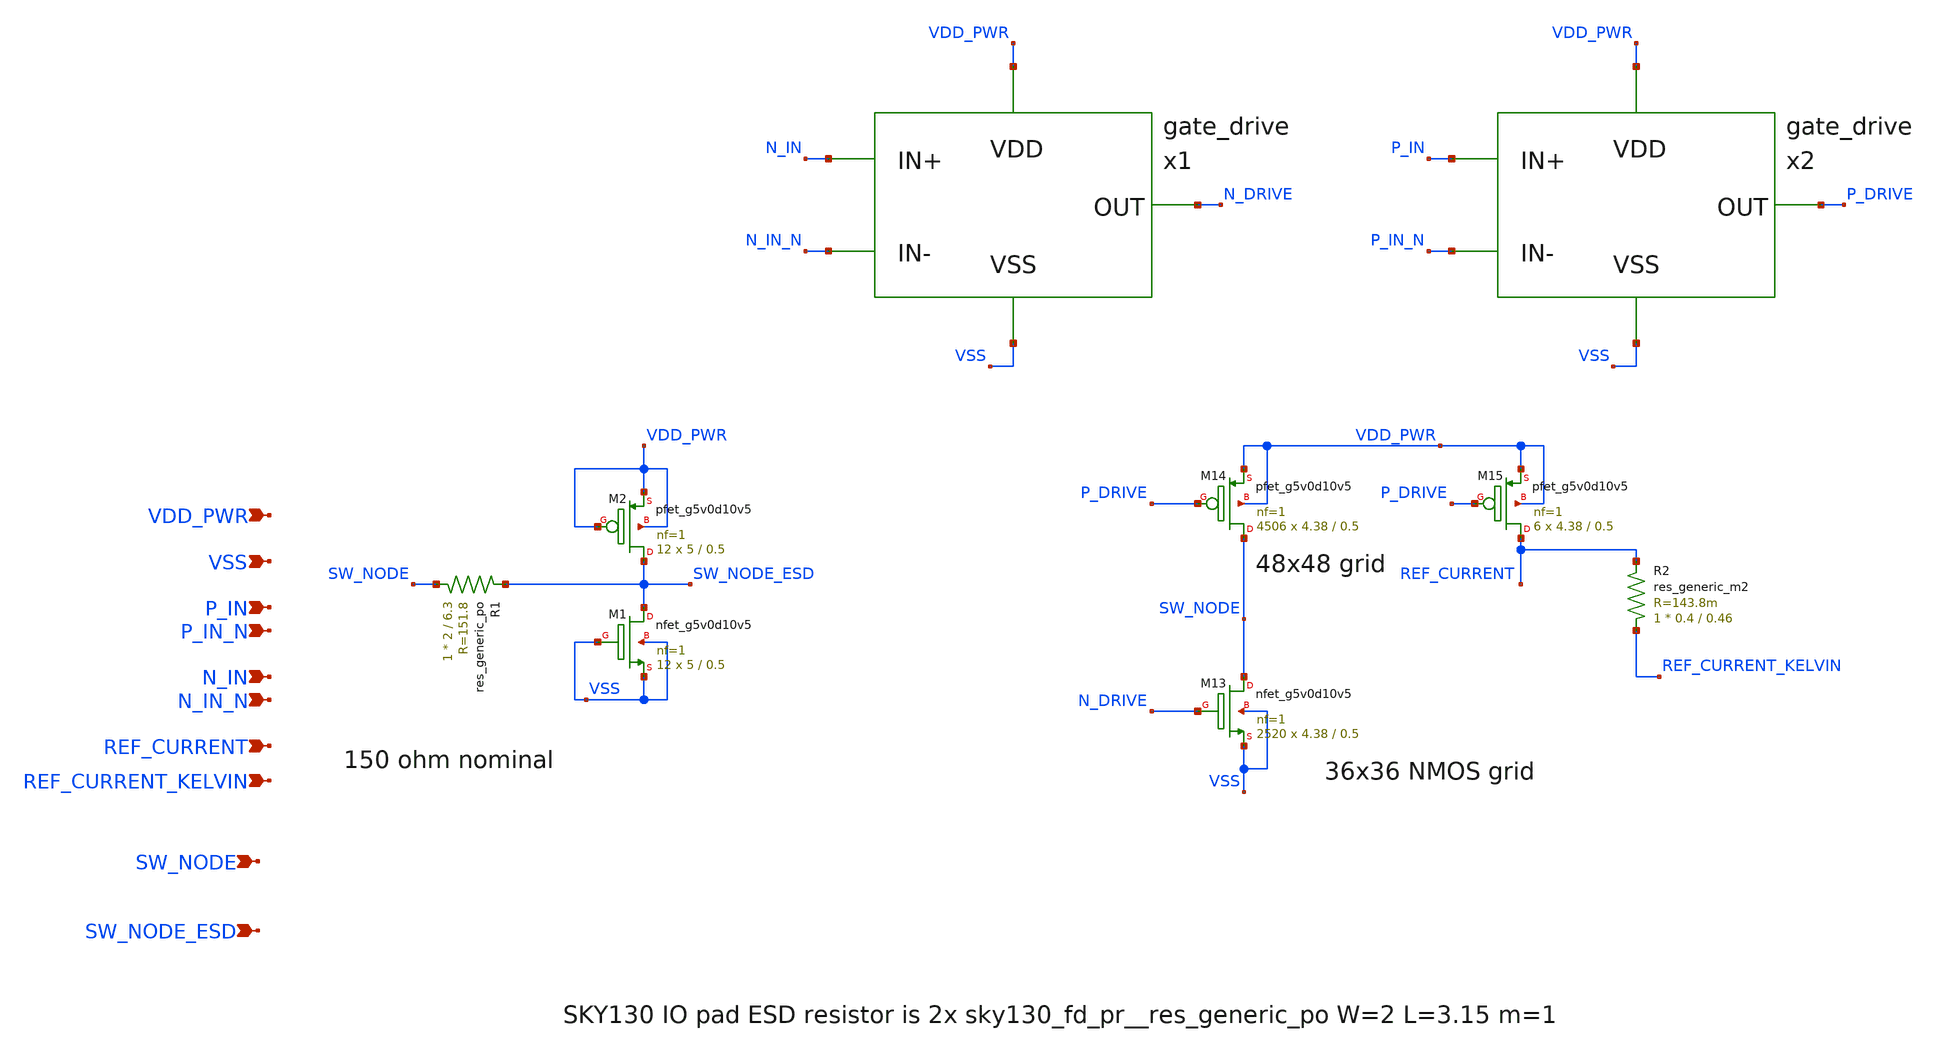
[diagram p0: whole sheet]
** sch_path: images/foss-asic-tools/addons/examples/open-pmic/design/power-stage/power_stage.sch
**.subckt power_stage N_IN VSS P_IN P_IN_N N_IN_N VDD_PWR REF_CURRENT SW_NODE SW_NODE_ESD
*+ REF_CURRENT_KELVIN
*.ipin N_IN
*.ipin VSS
*.ipin P_IN
*.ipin P_IN_N
*.ipin N_IN_N
*.ipin VDD_PWR
*.ipin REF_CURRENT
*.ipin SW_NODE
*.ipin SW_NODE_ESD
*.ipin REF_CURRENT_KELVIN
XM13 SW_NODE N_DRIVE VSS VSS sky130_fd_pr__nfet_g5v0d10v5 L=0.5 W=4.38 nf=1 ad='int((nf+1)/2) * W/nf * 0.29'
+ as='int((nf+2)/2) * W/nf * 0.29' pd='2*int((nf+1)/2) * (W/nf + 0.29)' ps='2*int((nf+2)/2) * (W/nf + 0.29)'
+ nrd='0.29 / W' nrs='0.29 / W' sa=0 sb=0 sd=0 mult=2520 m=2520
XM14 SW_NODE P_DRIVE VDD_PWR VDD_PWR sky130_fd_pr__pfet_g5v0d10v5 L=0.5 W=4.38 nf=1 ad='int((nf+1)/2) * W/nf * 0.29'
+ as='int((nf+2)/2) * W/nf * 0.29' pd='2*int((nf+1)/2) * (W/nf + 0.29)' ps='2*int((nf+2)/2) * (W/nf + 0.29)'
+ nrd='0.29 / W' nrs='0.29 / W' sa=0 sb=0 sd=0 mult=4506 m=4506
XM15 REF_CURRENT P_DRIVE VDD_PWR VDD_PWR sky130_fd_pr__pfet_g5v0d10v5 L=0.5 W=4.38 nf=1 ad='int((nf+1)/2) * W/nf * 0.29'
+ as='int((nf+2)/2) * W/nf * 0.29' pd='2*int((nf+1)/2) * (W/nf + 0.29)' ps='2*int((nf+2)/2) * (W/nf + 0.29)'
+ nrd='0.29 / W' nrs='0.29 / W' sa=0 sb=0 sd=0 mult=6 m=6
x1 N_IN N_IN_N VDD_PWR VSS N_DRIVE gate_drive
x2 P_IN P_IN_N VDD_PWR VSS P_DRIVE gate_drive
XM1 SW_NODE_ESD VSS VSS VSS sky130_fd_pr__nfet_g5v0d10v5 L=0.5 W=5 nf=1 ad='int((nf+1)/2) * W/nf * 0.29'
+ as='int((nf+2)/2) * W/nf * 0.29' pd='2*int((nf+1)/2) * (W/nf + 0.29)' ps='2*int((nf+2)/2) * (W/nf + 0.29)'
+ nrd='0.29 / W' nrs='0.29 / W' sa=0 sb=0 sd=0 mult=12 m=12
XM2 SW_NODE_ESD VDD_PWR VDD_PWR VDD_PWR sky130_fd_pr__pfet_g5v0d10v5 L=0.5 W=5 nf=1 ad='int((nf+1)/2) * W/nf * 0.29'
+ as='int((nf+2)/2) * W/nf * 0.29' pd='2*int((nf+1)/2) * (W/nf + 0.29)' ps='2*int((nf+2)/2) * (W/nf + 0.29)'
+ nrd='0.29 / W' nrs='0.29 / W' sa=0 sb=0 sd=0 mult=12 m=12
XR1 SW_NODE SW_NODE_ESD sky130_fd_pr__res_generic_po W=2 L=6.3 m=1
R2 REF_CURRENT_KELVIN REF_CURRENT sky130_fd_pr__res_generic_m2 W=0.4 L=0.46 m=1
**.ends
.end
